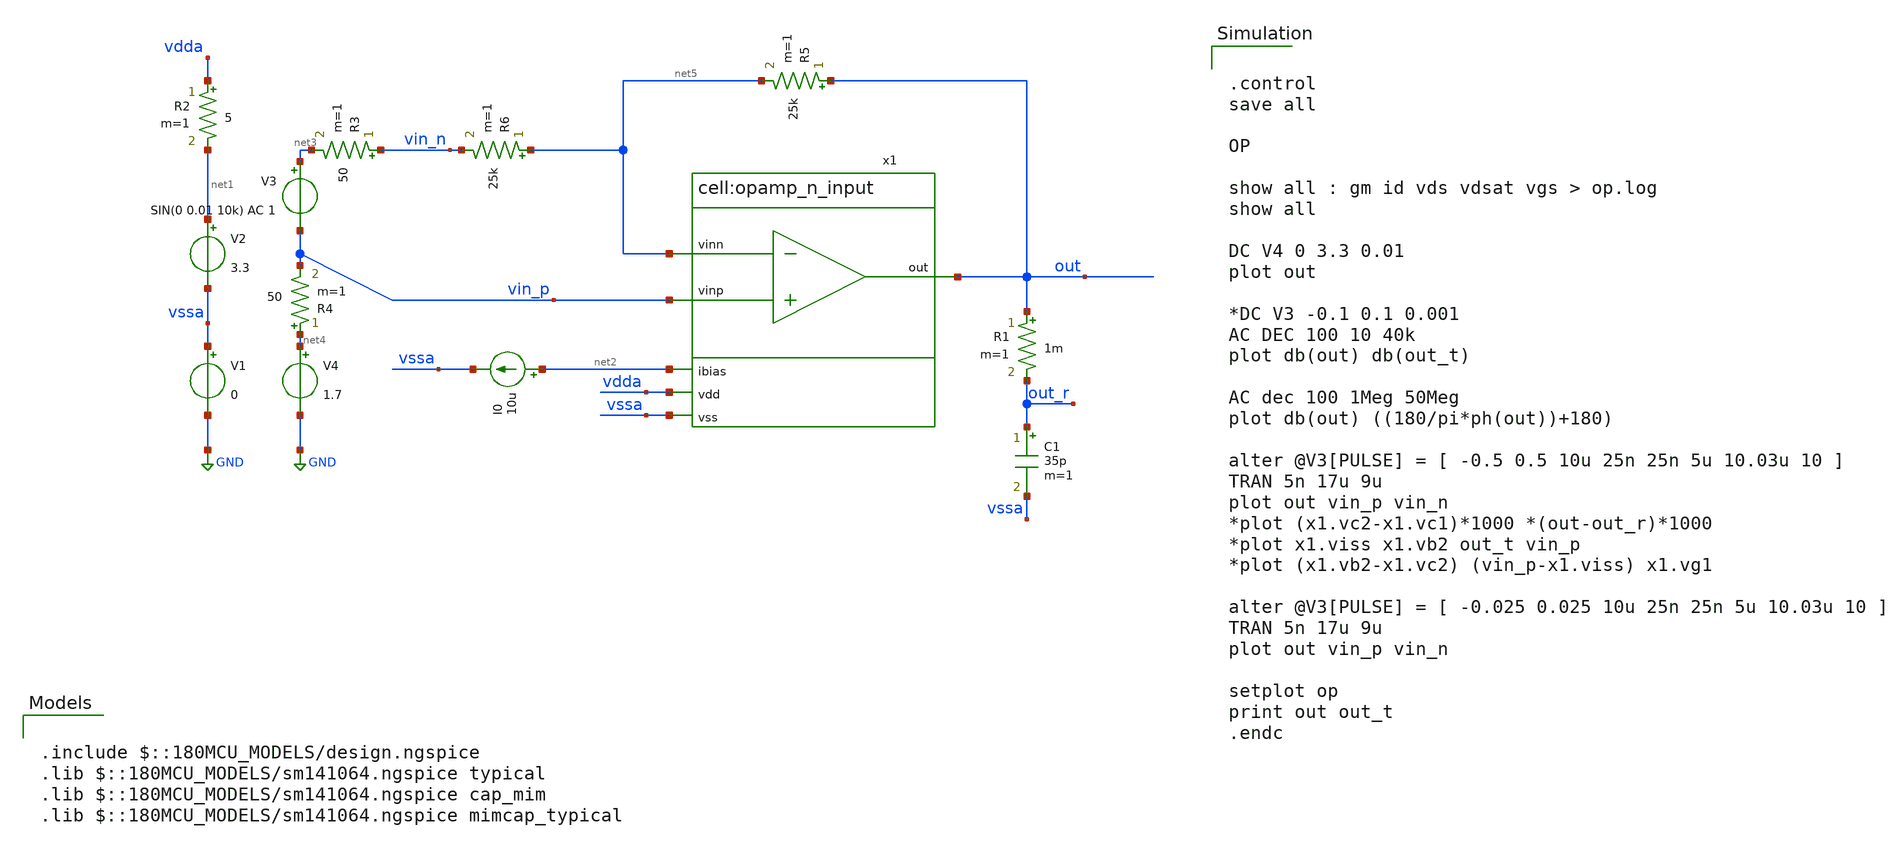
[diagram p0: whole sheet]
** sch_path: designs/libs/tb_analog/opamp/opamp_n_tb.sch
**.subckt opamp_n_tb
x1 vin_p net5 net2 vdda out vssa opamp_n_input
V1 vssa GND 0
V2 net1 vssa 3.3
I0 net2 vssa 10u
V3 net3 vin_p SIN(0 0.01 10k) AC 1
V4 net4 GND 1.7
C1 out_r vssa 35p m=1
R1 out out_r 1m m=1
R2 vdda net1 5 m=1
R3 vin_n net3 50 m=1
R4 net4 vin_p 50 m=1
R5 out net5 25k m=1
R6 net5 vin_n 25k m=1
**** begin user architecture code


.control
save all

OP

show all : gm id vds vdsat vgs > op.log
show all

DC V4 0 3.3 0.01
plot out

*DC V3 -0.1 0.1 0.001
AC DEC 100 10 40k
plot db(out) db(out_t)

AC dec 100 1Meg 50Meg
plot db(out) ((180/pi*ph(out))+180)

alter @V3[PULSE] = [ -0.5 0.5 10u 25n 25n 5u 10.03u 10 ]
TRAN 5n 17u 9u
plot out vin_p vin_n
*plot (x1.vc2-x1.vc1)*1000 *(out-out_r)*1000
*plot x1.viss x1.vb2 out_t vin_p
*plot (x1.vb2-x1.vc2) (vin_p-x1.viss) x1.vg1

alter @V3[PULSE] = [ -0.025 0.025 10u 25n 25n 5u 10.03u 10 ]
TRAN 5n 17u 9u
plot out vin_p vin_n

setplot op
print out out_t
.endc



.include $::180MCU_MODELS/design.ngspice
.lib $::180MCU_MODELS/sm141064.ngspice typical
.lib $::180MCU_MODELS/sm141064.ngspice cap_mim
.lib $::180MCU_MODELS/sm141064.ngspice mimcap_typical

**** end user architecture code
**.ends

* expanding   symbol:  libs/core_analog/opamp/opamp_n_input.sym # of pins=6
** sym_path: libs/core_analog/opamp/opamp_n_input.sym
** sch_path: libs/core_analog/opamp/opamp_n_input.sch
.subckt opamp_n_input vinp vinn ibias vdd out vss
*.opin out
*.ipin vdd
*.ipin vss
*.ipin vinn
*.ipin ibias
*.ipin vinp
XM1 net1 vinn viss vss nfet_03v3 L=1u W=3u nf=1 ad='int((nf+1)/2) * W/nf * 0.18u' as='int((nf+2)/2) * W/nf * 0.18u'
+ pd='2*int((nf+1)/2) * (W/nf + 0.18u)' ps='2*int((nf+2)/2) * (W/nf + 0.18u)' nrd='0.18u / W' nrs='0.18u / W'
+ sa=0 sb=0 sd=0 m=1
XM2 net2 vinp viss vss nfet_03v3 L=1u W=3u nf=1 ad='int((nf+1)/2) * W/nf * 0.18u' as='int((nf+2)/2) * W/nf * 0.18u'
+ pd='2*int((nf+1)/2) * (W/nf + 0.18u)' ps='2*int((nf+2)/2) * (W/nf + 0.18u)' nrd='0.18u / W' nrs='0.18u / W'
+ sa=0 sb=0 sd=0 m=1
XM6 net3 vg1 vdd vdd pfet_03v3 L=0.8u W=5u nf=1 ad='int((nf+1)/2) * W/nf * 0.18u' as='int((nf+2)/2) * W/nf * 0.18u'
+ pd='2*int((nf+1)/2) * (W/nf + 0.18u)' ps='2*int((nf+2)/2) * (W/nf + 0.18u)' nrd='0.18u / W' nrs='0.18u / W'
+ sa=0 sb=0 sd=0 m=5
XM5 vg1 vg1 vdd vdd pfet_03v3 L=0.8u W=5u nf=1 ad='int((nf+1)/2) * W/nf * 0.18u' as='int((nf+2)/2) * W/nf * 0.18u'
+ pd='2*int((nf+1)/2) * (W/nf + 0.18u)' ps='2*int((nf+2)/2) * (W/nf + 0.18u)' nrd='0.18u / W' nrs='0.18u / W'
+ sa=0 sb=0 sd=0 m=5
XM4 net3 vb2 net2 vss nfet_03v3 L=1u W=5u nf=1 ad='int((nf+1)/2) * W/nf * 0.18u' as='int((nf+2)/2) * W/nf * 0.18u'
+ pd='2*int((nf+1)/2) * (W/nf + 0.18u)' ps='2*int((nf+2)/2) * (W/nf + 0.18u)' nrd='0.18u / W' nrs='0.18u / W'
+ sa=0 sb=0 sd=0 m=6
XM3 vg1 vb2 net1 vss nfet_03v3 L=1u W=5u nf=1 ad='int((nf+1)/2) * W/nf * 0.18u' as='int((nf+2)/2) * W/nf * 0.18u'
+ pd='2*int((nf+1)/2) * (W/nf + 0.18u)' ps='2*int((nf+2)/2) * (W/nf + 0.18u)' nrd='0.18u / W' nrs='0.18u / W'
+ sa=0 sb=0 sd=0 m=6
XM7 viss net4 vss vss nfet_03v3 L=2u W=4.5u nf=1 ad='int((nf+1)/2) * W/nf * 0.18u' as='int((nf+2)/2) * W/nf * 0.18u'
+ pd='2*int((nf+1)/2) * (W/nf + 0.18u)' ps='2*int((nf+2)/2) * (W/nf + 0.18u)' nrd='0.18u / W' nrs='0.18u / W'
+ sa=0 sb=0 sd=0 m=3
XM11 net4 net4 vss vss nfet_03v3 L=2u W=4.5u nf=1 ad='int((nf+1)/2) * W/nf * 0.18u' as='int((nf+2)/2) * W/nf * 0.18u'
+ pd='2*int((nf+1)/2) * (W/nf + 0.18u)' ps='2*int((nf+2)/2) * (W/nf + 0.18u)' nrd='0.18u / W' nrs='0.18u / W'
+ sa=0 sb=0 sd=0 m=1
XM10 vb2 vb2 viss vss nfet_03v3 L=4u W=2u nf=1 ad='int((nf+1)/2) * W/nf * 0.18u' as='int((nf+2)/2) * W/nf * 0.18u'
+ pd='2*int((nf+1)/2) * (W/nf + 0.18u)' ps='2*int((nf+2)/2) * (W/nf + 0.18u)' nrd='0.18u / W' nrs='0.18u / W'
+ sa=0 sb=0 sd=0 m=1
XM8 out net4 vss vss nfet_03v3 L=0.8u W=5.5u nf=1 ad='int((nf+1)/2) * W/nf * 0.18u' as='int((nf+2)/2) * W/nf * 0.18u'
+ pd='2*int((nf+1)/2) * (W/nf + 0.18u)' ps='2*int((nf+2)/2) * (W/nf + 0.18u)' nrd='0.18u / W' nrs='0.18u / W'
+ sa=0 sb=0 sd=0 m=2
XM9 out net3 vdd vdd pfet_03v3 L=0.5u W=5.5u nf=1 ad='int((nf+1)/2) * W/nf * 0.18u' as='int((nf+2)/2) * W/nf * 0.18u'
+ pd='2*int((nf+1)/2) * (W/nf + 0.18u)' ps='2*int((nf+2)/2) * (W/nf + 0.18u)' nrd='0.18u / W' nrs='0.18u / W'
+ sa=0 sb=0 sd=0 m=14
XM12 net7 net7 net4 vss nfet_03v3 L=2u W=4.5u nf=1 ad='int((nf+1)/2) * W/nf * 0.18u' as='int((nf+2)/2) * W/nf * 0.18u'
+ pd='2*int((nf+1)/2) * (W/nf + 0.18u)' ps='2*int((nf+2)/2) * (W/nf + 0.18u)' nrd='0.18u / W' nrs='0.18u / W'
+ sa=0 sb=0 sd=0 m=1
XM13 vb2 net5 vdd vdd pfet_03v3 L=1u W=3.5u nf=1 ad='int((nf+1)/2) * W/nf * 0.18u' as='int((nf+2)/2) * W/nf * 0.18u'
+ pd='2*int((nf+1)/2) * (W/nf + 0.18u)' ps='2*int((nf+2)/2) * (W/nf + 0.18u)' nrd='0.18u / W' nrs='0.18u / W'
+ sa=0 sb=0 sd=0 m=1
XM14 net5 net5 vdd vdd pfet_03v3 L=1u W=3.5u nf=1 ad='int((nf+1)/2) * W/nf * 0.18u' as='int((nf+2)/2) * W/nf * 0.18u'
+ pd='2*int((nf+1)/2) * (W/nf + 0.18u)' ps='2*int((nf+2)/2) * (W/nf + 0.18u)' nrd='0.18u / W' nrs='0.18u / W'
+ sa=0 sb=0 sd=0 m=1
XM15 ibias ibias net5 vdd pfet_03v3 L=1u W=3.5u nf=1 ad='int((nf+1)/2) * W/nf * 0.18u' as='int((nf+2)/2) * W/nf * 0.18u'
+ pd='2*int((nf+1)/2) * (W/nf + 0.18u)' ps='2*int((nf+2)/2) * (W/nf + 0.18u)' nrd='0.18u / W' nrs='0.18u / W'
+ sa=0 sb=0 sd=0 m=1
XM16 net7 ibias net6 vdd pfet_03v3 L=1u W=3.5u nf=1 ad='int((nf+1)/2) * W/nf * 0.18u' as='int((nf+2)/2) * W/nf * 0.18u'
+ pd='2*int((nf+1)/2) * (W/nf + 0.18u)' ps='2*int((nf+2)/2) * (W/nf + 0.18u)' nrd='0.18u / W' nrs='0.18u / W'
+ sa=0 sb=0 sd=0 m=1
XM17 net6 net5 vdd vdd pfet_03v3 L=1u W=3.5u nf=1 ad='int((nf+1)/2) * W/nf * 0.18u' as='int((nf+2)/2) * W/nf * 0.18u'
+ pd='2*int((nf+1)/2) * (W/nf + 0.18u)' ps='2*int((nf+2)/2) * (W/nf + 0.18u)' nrd='0.18u / W' nrs='0.18u / W'
+ sa=0 sb=0 sd=0 m=1
XC2 net2 out cap_mim_2f0_m5m6_noshield c_width=25e-6 c_length=24e-6 m=1
.ends

.GLOBAL GND
.end
